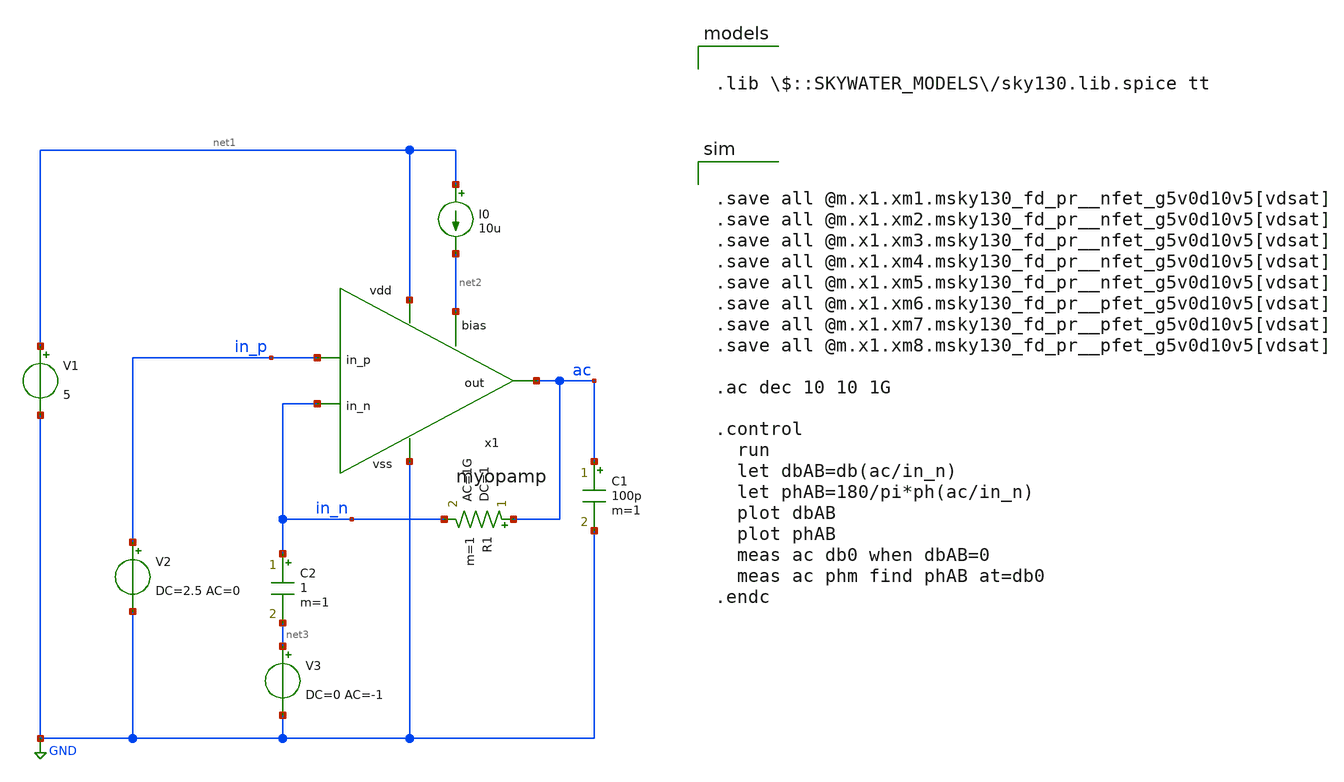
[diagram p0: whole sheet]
** sch_path: design/myopamp/test/ac_tb.sch
**.subckt ac_tb
x1 net1 in_n in_p ac net2 GND myopamp
V1 net1 GND 5
I0 net1 net2 10u
V3 net3 GND DC=0 AC=-1
C1 ac GND 100p m=1
R1 ac in_n 1 ac=1G m=1
C2 in_n net3 1 m=1
V2 in_p GND DC=2.5 AC=0
**** begin user architecture code


.save all @m.x1.xm1.msky130_fd_pr__nfet_g5v0d10v5[vdsat]
.save all @m.x1.xm2.msky130_fd_pr__nfet_g5v0d10v5[vdsat]
.save all @m.x1.xm3.msky130_fd_pr__nfet_g5v0d10v5[vdsat]
.save all @m.x1.xm4.msky130_fd_pr__nfet_g5v0d10v5[vdsat]
.save all @m.x1.xm5.msky130_fd_pr__nfet_g5v0d10v5[vdsat]
.save all @m.x1.xm6.msky130_fd_pr__pfet_g5v0d10v5[vdsat]
.save all @m.x1.xm7.msky130_fd_pr__pfet_g5v0d10v5[vdsat]
.save all @m.x1.xm8.msky130_fd_pr__pfet_g5v0d10v5[vdsat]

.ac dec 10 10 1G

.control
  run
  let dbAB=db(ac/in_n)
  let phAB=180/pi*ph(ac/in_n)
  plot dbAB
  plot phAB
  meas ac db0 when dbAB=0
  meas ac phm find phAB at=db0
.endc



.lib $::SKYWATER_MODELS/sky130.lib.spice tt

**** end user architecture code
**.ends

* expanding   symbol:  myopamp/myopamp.sym # of pins=6
** sym_path: design/myopamp/myopamp.sym
** sch_path: design/myopamp/myopamp.sch
.subckt myopamp vdd in_n in_p out bias vss
*.ipin in_n
*.ipin in_p
*.ipin bias
*.opin out
*.iopin vdd
*.iopin vss
XM7 vdd net2 net3 vdd sky130_fd_pr__pfet_g5v0d10v5 L=2 W=2 nf=1 ad='int((nf+1)/2) * W/nf * 0.29' as='int((nf+2)/2) * W/nf * 0.29'
+ pd='2*int((nf+1)/2) * (W/nf + 0.29)' ps='2*int((nf+2)/2) * (W/nf + 0.29)' nrd='0.29 / W' nrs='0.29 / W'
+ sa=0 sb=0 sd=0 mult=2 m=2
XM6 vdd net2 net2 vdd sky130_fd_pr__pfet_g5v0d10v5 L=2 W=2 nf=1 ad='int((nf+1)/2) * W/nf * 0.29' as='int((nf+2)/2) * W/nf * 0.29'
+ pd='2*int((nf+1)/2) * (W/nf + 0.29)' ps='2*int((nf+2)/2) * (W/nf + 0.29)' nrd='0.29 / W' nrs='0.29 / W'
+ sa=0 sb=0 sd=0 mult=2 m=2
XM8 vdd net3 out vdd sky130_fd_pr__pfet_g5v0d10v5 L=2 W=2 nf=1 ad='int((nf+1)/2) * W/nf * 0.29' as='int((nf+2)/2) * W/nf * 0.29'
+ pd='2*int((nf+1)/2) * (W/nf + 0.29)' ps='2*int((nf+2)/2) * (W/nf + 0.29)' nrd='0.29 / W' nrs='0.29 / W'
+ sa=0 sb=0 sd=0 mult=16 m=16
XM4 net2 in_n net1 vss sky130_fd_pr__nfet_g5v0d10v5 L=1 W=10 nf=1 ad='int((nf+1)/2) * W/nf * 0.29' as='int((nf+2)/2) * W/nf * 0.29'
+ pd='2*int((nf+1)/2) * (W/nf + 0.29)' ps='2*int((nf+2)/2) * (W/nf + 0.29)' nrd='0.29 / W' nrs='0.29 / W'
+ sa=0 sb=0 sd=0 mult=10 m=10
XM5 net3 in_p net1 vss sky130_fd_pr__nfet_g5v0d10v5 L=1 W=10 nf=1 ad='int((nf+1)/2) * W/nf * 0.29' as='int((nf+2)/2) * W/nf * 0.29'
+ pd='2*int((nf+1)/2) * (W/nf + 0.29)' ps='2*int((nf+2)/2) * (W/nf + 0.29)' nrd='0.29 / W' nrs='0.29 / W'
+ sa=0 sb=0 sd=0 mult=10 m=10
XM1 bias bias vss vss sky130_fd_pr__nfet_g5v0d10v5 L=2 W=1 nf=1 ad='int((nf+1)/2) * W/nf * 0.29' as='int((nf+2)/2) * W/nf * 0.29'
+ pd='2*int((nf+1)/2) * (W/nf + 0.29)' ps='2*int((nf+2)/2) * (W/nf + 0.29)' nrd='0.29 / W' nrs='0.29 / W'
+ sa=0 sb=0 sd=0 mult=2 m=2
XM2 net1 bias vss vss sky130_fd_pr__nfet_g5v0d10v5 L=2 W=1 nf=1 ad='int((nf+1)/2) * W/nf * 0.29' as='int((nf+2)/2) * W/nf * 0.29'
+ pd='2*int((nf+1)/2) * (W/nf + 0.29)' ps='2*int((nf+2)/2) * (W/nf + 0.29)' nrd='0.29 / W' nrs='0.29 / W'
+ sa=0 sb=0 sd=0 mult=2 m=2
XM3 out bias vss vss sky130_fd_pr__nfet_g5v0d10v5 L=2 W=1 nf=1 ad='int((nf+1)/2) * W/nf * 0.29' as='int((nf+2)/2) * W/nf * 0.29'
+ pd='2*int((nf+1)/2) * (W/nf + 0.29)' ps='2*int((nf+2)/2) * (W/nf + 0.29)' nrd='0.29 / W' nrs='0.29 / W'
+ sa=0 sb=0 sd=0 mult=16 m=16
XC1 net3 net4 sky130_fd_pr__cap_mim_m3_1 W=30 L=30 MF=6 m=6
XR1 out net4 vss sky130_fd_pr__res_xhigh_po W=0.69 L=10 mult=1 m=1
.ends

.GLOBAL GND
.end
